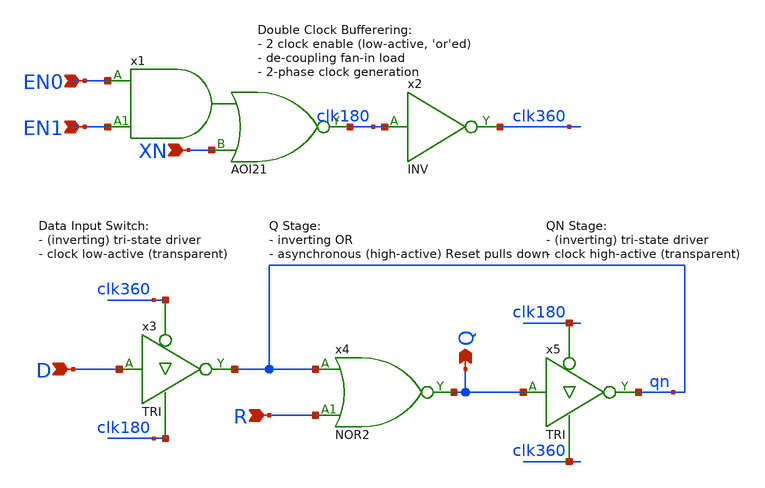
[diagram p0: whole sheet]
** sch_path: Sources/crafted/LATNEER.sch
**.subckt LATNEER XN D Q EN0 EN1 R
*.ipin XN
*.ipin D
*.opin Q
*.ipin EN0
*.ipin EN1
*.ipin R
x1 EN0 EN1 XN clk180 VDD GND AOI21 Wmin=1.5u Lmin=1u g=2 m=1
x2 clk180 clk360 VDD GND INV Wmin=1.5u Lmin=1u g=2 m=1
x4 qn R Q VDD GND NOR2 Wmin=1.5u Lmin=1u g=2 m=1
x3 D clk360 clk180 qn VDD GND TRI Wmin=1.5u Lmin=1u g=2 m=1
x5 Q clk180 clk360 qn VDD GND TRI Wmin=1.5u Lmin=1u g=2 m=1
**.ends
.end
